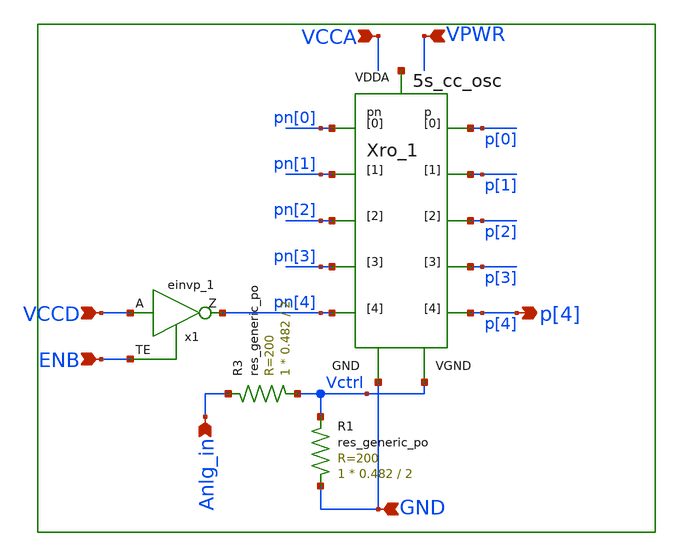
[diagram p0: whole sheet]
** sch_path: xschem/lib/vco.sch
**.subckt vco Anlg_in p[4] VCCA VCCD ENB VPWR GND
*.ipin Anlg_in
*.opin p[4]
*.ipin VCCA
*.ipin VCCD
*.ipin ENB
*.ipin VPWR
*.ipin GND
x1 VCCD ENB GND GND VCCD VCCD pn[4] sky130_fd_sc_hd__einvp_1
Xro_1 Vctrl net1 p[0] p[1] p[2] p[3] p[4] pn[0] pn[1] pn[2] pn[3] pn[4] GND 5s_cc_osc
XR3 Vctrl Anlg_in sky130_fd_pr__res_generic_po W=0.482 L=2 m=1
XR1 GND Vctrl sky130_fd_pr__res_generic_po W=0.482 L=2 m=1
**.ends
.end
